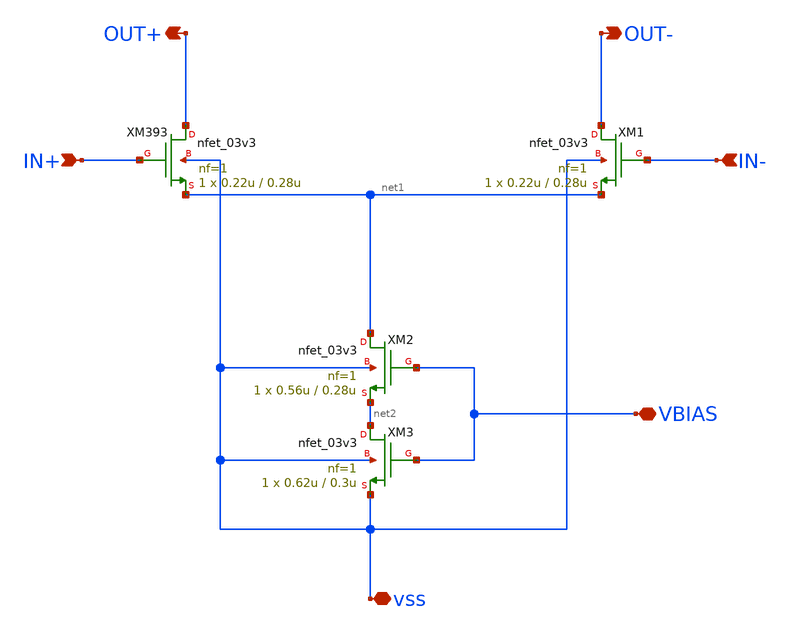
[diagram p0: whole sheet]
** sch_path: xschem/CS_Switch_8x.sch
**.subckt CS_Switch_8x OUT+ OUT- IN+ IN- VBIAS vss
*.opin OUT+
*.opin OUT-
*.ipin IN+
*.ipin IN-
*.iopin VBIAS
*.iopin vss
XM393 OUT+ IN+ net1 vss nfet_03v3 L=0.28u W=0.22u nf=1 ad='int((nf+1)/2) * W/nf * 0.18u' as='int((nf+2)/2) * W/nf * 0.18u'
+ pd='2*int((nf+1)/2) * (W/nf + 0.18u)' ps='2*int((nf+2)/2) * (W/nf + 0.18u)' nrd='0.18u / W' nrs='0.18u / W'
+ sa=0 sb=0 sd=0 m=1
XM2 net1 VBIAS net2 vss nfet_03v3 L=0.28u W=0.56u nf=1 ad='int((nf+1)/2) * W/nf * 0.18u' as='int((nf+2)/2) * W/nf * 0.18u'
+ pd='2*int((nf+1)/2) * (W/nf + 0.18u)' ps='2*int((nf+2)/2) * (W/nf + 0.18u)' nrd='0.18u / W' nrs='0.18u / W'
+ sa=0 sb=0 sd=0 m=1
XM3 net2 VBIAS vss vss nfet_03v3 L=0.3u W=0.62u nf=1 ad='int((nf+1)/2) * W/nf * 0.18u' as='int((nf+2)/2) * W/nf * 0.18u'
+ pd='2*int((nf+1)/2) * (W/nf + 0.18u)' ps='2*int((nf+2)/2) * (W/nf + 0.18u)' nrd='0.18u / W' nrs='0.18u / W'
+ sa=0 sb=0 sd=0 m=1
XM1 OUT- IN- net1 vss nfet_03v3 L=0.28u W=0.22u nf=1 ad='int((nf+1)/2) * W/nf * 0.18u' as='int((nf+2)/2) * W/nf * 0.18u'
+ pd='2*int((nf+1)/2) * (W/nf + 0.18u)' ps='2*int((nf+2)/2) * (W/nf + 0.18u)' nrd='0.18u / W' nrs='0.18u / W'
+ sa=0 sb=0 sd=0 m=1
**.ends
.end
